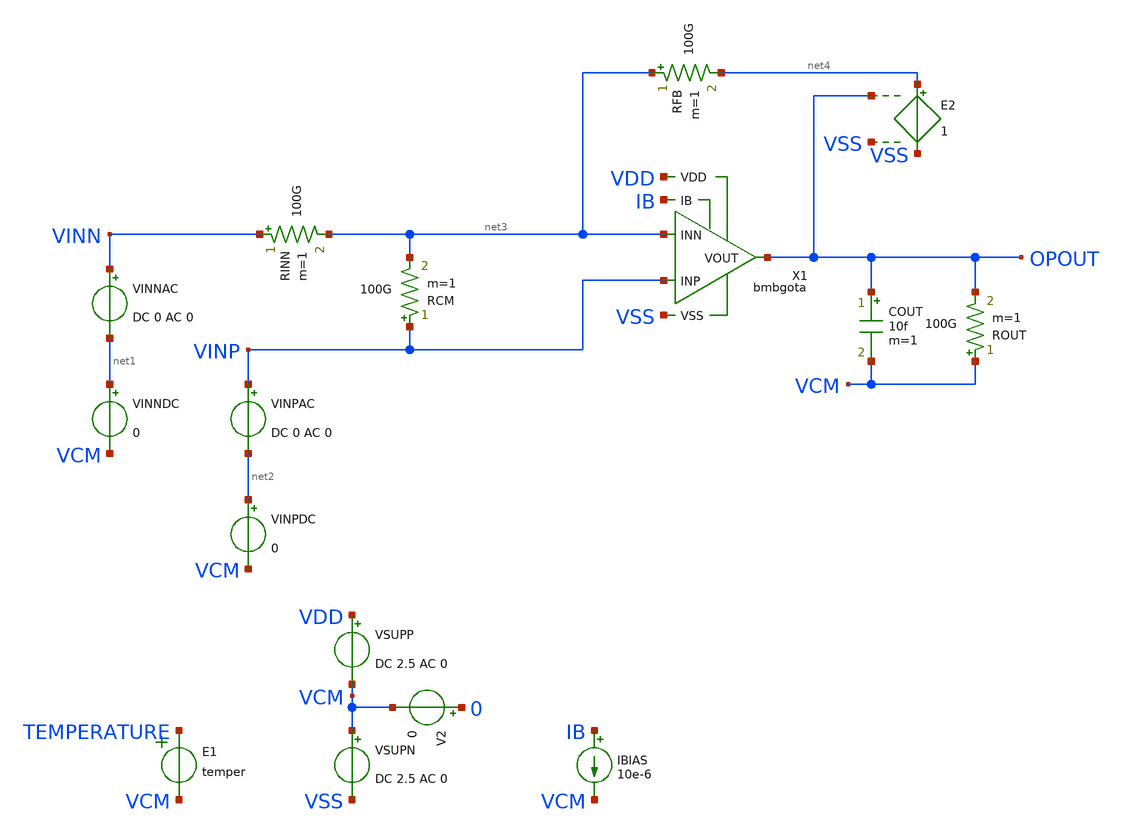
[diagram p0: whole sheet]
** sch_path: tt08/ip/bmbg/xschem/bmbgota_tb.sch
**.subckt bmbgota_tb
V2 0 VCM 0
E1 TEMPERATURE VCM VOL=' temper '
X1 VDD VSS OPOUT IB net3 VINP bmbgota
IBIAS IB VCM 10e-6
COUT OPOUT VCM 10f m=1
VINNDC net1 VCM 0
VINNAC VINN net1 DC 0 AC 0
VINPDC net2 VCM 0
VINPAC VINP net2 DC 0 AC 0
ROUT VCM OPOUT 100G m=1
VSUPP VDD VCM DC 2.5 AC 0
RFB net3 net4 100G m=1
RINN VINN net3 100G m=1
RCM VINP net3 100G m=1
VSUPN VCM VSS DC 2.5 AC 0
E2 net4 VSS OPOUT VSS 1
**** begin user architecture code

.csparam TB_ID=$::TB_ID\
.csparam MC_RUNS=$::MC_RUNS\
.csparam EXIT_NGSPICE=$::EXIT_NGSPICE\
.lib $::SKYWATER_MODELS/sky130.lib.spice $::CORNER\


* this experimental option enables mos model bin
* selection based on W/NF instead of W
.option wnflag=0

.control
* option savecurrents

* dummy block for goto
if (1)
if TB_ID = 0
	goto AC_OL
end
if TB_ID = 1
	goto AC_OL
end
if TB_ID = 2
	goto AC_CMRR_PSRR
end
if TB_ID = 3
	goto TRAN_OUTRNG
end
if TB_ID = 4
	goto TRAN_CMINP
end
if TB_ID = 5
	goto TRAN_SLEW
end
if TB_ID = 6
	goto AC_INOISE
end
if TB_ID = 7
	goto TRAN_THD
end

* Helper Functions
******************
define aunif(nom, avar) (nom+avar*sunif(0))
define agauss(nom, avar, sig) (nom + avar / sig * sgauss (0))

****************************************
label AC_OL
save all
****************************************
if MC_RUNS = 0
	let olgain_1hz = vector(MC_RUNS+1)
	let pm = vector(MC_RUNS+1)
	let ugbw = vector(MC_RUNS+1)
	let f1_3db = vector(MC_RUNS+1)
	let f2_3db = vector(MC_RUNS+1)
	let run=0

	.include ac_ol_ops.inc

	set nobreak
	set width=300
	print col olgain_1hz, pm, ugbw, f1_3db, f2_3db > ac_ol.csv
else
	let olgain_1hz = vector(MC_RUNS)
	let pm = vector(MC_RUNS)
	let ugbw = vector(MC_RUNS)
	let f1_3db = vector(MC_RUNS)
	let f2_3db = vector(MC_RUNS)
	let run=0
	dowhile run < MC_RUNS
		echo MC-RUN: $&run

		.include ac_ol_ops.inc

 		reset
		let run = run + 1
	end
	set nobreak
	set width=300
	print olgain_1hz, pm, ugbw, f1_3db, f2_3db > ac_ol.csv
end
goto done

****************************************
label AC_CMRR_PSRR
save all
****************************************
if MC_RUNS = 0
	let cmrr_10Hz = vector(MC_RUNS+1)
	let cmrr_10MHz = vector(MC_RUNS+1)
	let psrr_p_10Hz = vector(MC_RUNS+1)
	let psrr_p_10MHz = vector(MC_RUNS+1)
	let psrr_n_10Hz = vector(MC_RUNS+1)
	let psrr_n_10MHz = vector(MC_RUNS+1)
	let run=0

	.include ac_cmrr_psrr_ops.inc

	set nobreak
	set width=300
	print col cmrr_10Hz, cmrr_10MHz, psrr_p_10Hz, psrr_p_10MHz, psrr_n_10Hz, psrr_n_10MHz >
+ ac_cmrr_psrr.csv
else
	let cmrr_10Hz = vector(MC_RUNS)
	let cmrr_10MHz = vector(MC_RUNS)
	let psrr_p_10Hz = vector(MC_RUNS)
	let psrr_p_10MHz = vector(MC_RUNS)
	let psrr_n_10Hz = vector(MC_RUNS)
	let psrr_n_10MHz = vector(MC_RUNS)
	let run=0
	dowhile run < MC_RUNS
		echo MC-RUN: $&run

		.include ac_cmrr_psrr_ops.inc

 		reset
		let run = run + 1
	end
	set nobreak
	set width=300
	print cmrr_10Hz, cmrr_10MHz, psrr_p_10Hz, psrr_p_10MHz, psrr_n_10Hz, psrr_n_10MHz >
+ ac_cmrr_psrr.csv
end
goto done

****************************************
label TRAN_OUTRNG
save all
****************************************
if MC_RUNS = 0
	let neg_out_comp = vector(MC_RUNS+1)
	let pos_out_comp = vector(MC_RUNS+1)
	let run=0

	.include tran_outrng_ops.inc

	set nobreak
	set width=300
	print col neg_out_comp, pos_out_comp > tran_outrng.csv
else
	let neg_out_comp = vector(MC_RUNS)
	let pos_out_comp = vector(MC_RUNS)
	let run=0
	dowhile run < MC_RUNS
		echo MC-RUN: $&run

		.include tran_outrng_ops.inc

 		reset
		let run = run + 1
	end
	set nobreak
	set width=300
	print neg_out_comp, pos_out_comp > tran_outrng.csv
end
goto done

****************************************
label TRAN_CMINP
save all
****************************************
if MC_RUNS = 0
	let pos_cm_bound = vector(MC_RUNS+1)
	let neg_cm_bound = vector(MC_RUNS+1)
	let run=0

	.include tran_cminp_ops.inc

	set nobreak
	set width=300
	print col pos_cm_bound, neg_cm_bound > tran_inprng.csv
else
	let pos_cm_bound = vector(MC_RUNS)
	let neg_cm_bound = vector(MC_RUNS)
	let run=0
	dowhile run < MC_RUNS
		echo MC-RUN: $&run

		.include tran_cminp_ops.inc

 		reset
		let run = run + 1
	end
	set nobreak
	set width=300
	print pos_cm_bound, neg_cm_bound > tran_inprng.csv
end
goto done

****************************************
label TRAN_SLEW
save all
****************************************
if MC_RUNS = 0
	let inp_offset = vector(MC_RUNS+1)
	let slew_pos = vector(MC_RUNS+1)
	let slew_neg = vector(MC_RUNS+1)
	let run=0

	.include tran_slew_ops.inc

	set nobreak
	set width=300
	print col inp_offset, slew_pos, slew_neg > tran_slew.csv
else
	let inp_offset = vector(MC_RUNS)
	let slew_pos = vector(MC_RUNS)
	let slew_neg = vector(MC_RUNS)
	let run=0
	dowhile run < MC_RUNS
		echo MC-RUN: $&run

		.include tran_slew_ops.inc

 		reset
		let run = run + 1
	end
	set nobreak
	set width=300
	print inp_offset, slew_pos, slew_neg > tran_slew.csv
end
goto done

****************************************
label AC_INOISE
****************************************
alter vsupp dc = 2.5
alter vsupp ac = 0
alter vsupn dc = 2.5
alter vsupn ac = 0
alter vinnac ac = 0
alter vinndc dc = 0
alter vinpac ac = 0
alter vinpdc dc = 0
alter rinn resistance = 100e12
alter rinn ac = 100e12
alter rcm resistance = 100e12
alter rcm ac = 100e12
alter rfb resistance = 0
alter rfb ac = 0.01

noise v(opout) vinpac dec 10 1 100e6 1
print noise2.onoise_total noise2.inoise_total
plot noise1.onoise_spectrum
plot noise1.inoise_spectrum
setplot noise1
write noise1_opout.raw all

* https://sourceforge.net/p/ngspice/discussion/120973/thread/2aa3e30f/ -- Holger Vogt
* script to read a specific y-value if x given
**********************************************
let f0 = vector(1)
let f1 = vector(1)
let n_f0 = vector(1)
let n_f1 = vector(1)
compose freq_list values 10 10e3
foreach freq_idx 0 1
	let freq = freq_list[$freq_idx]
	* find index where freqency is just above interesting value
	setplot noise1
	let nn = 0
	while frequency[nn] < freq
		let nn = nn + 1
	end
	* define vectors of frequncies and values just above and below
	* selected frequeny
	let fnn = frequency[nn]
	let nn1 = nn - 1
	let fnn1 = frequency[nn1]
	let snn = onoise_spectrum[nn]
	let snn1 = onoise_spectrum[nn1]
	*print vector values
	echo nn = $&nn  fnn = $&fnn  snn = $&snn
	echo nn1 = $&nn1  fnn1 = $&fnn1  snn1 = $&snn1
	*linear interpolation for exact frequency
	let newsnn = snn1 + (snn - snn1)/(fnn - fnn1)*(freq - fnn1)
	echo newfnn = $&freq  newsnn = $&newsnn
	if $freq_idx = 0
		let f0 = freq
		let n_f0 = newsnn
	end
	if $freq_idx = 1
		let f1 = freq
		let n_f1 = newsnn
	end
end
set nobreak
set width=300
set noprintscale
print col f0, n_f0, f1, n_f1 > ac_inoise.csv

goto done

****************************************
label TRAN_THD
save all
****************************************
if MC_RUNS = 0
	let thd = vector(MC_RUNS+1)
	let run=0

	.include tran_thd_ops.inc

	set nobreak
	set width=300
	print col thd > tran_thd.csv
else
	let thd = vector(MC_RUNS)
	let run=0
	dowhile run < MC_RUNS
		echo MC-RUN: $&run

		reset

		.include tran_thd_ops.inc

		let run = run + 1
	end
	set nobreak
	set width=300
	print thd > tran_thd.csv
end
goto done

****************************************
label done
****************************************
if EXIT_NGSPICE > 0.0
	exit
end
end
.endc


**** end user architecture code
**.ends

* expanding   symbol:  bmbgota.sym # of pins=6
** sym_path: bmbgota.sym
** sch_path: bmbgota.sch
.subckt bmbgota VDD VSS VOUT IB INN INP
*.iopin INP
*.iopin INN
*.iopin VOUT
*.opin IB
*.iopin VDD
*.iopin VSS
XMDR vr INP vt VDD sky130_fd_pr__pfet_g5v0d10v5 L=1 W=20 nf=1 ad='int((nf+1)/2) * W/nf * 0.29' as='int((nf+2)/2) * W/nf * 0.29'
+ pd='2*int((nf+1)/2) * (W/nf + 0.29)' ps='2*int((nf+2)/2) * (W/nf + 0.29)' nrd='0.29 / W' nrs='0.29 / W'
+ sa=0 sb=0 sd=0 mult=8 m=8
XMMIRL vl vl VSS VSS sky130_fd_pr__nfet_g5v0d10v5 L=2 W=5 nf=1 ad='int((nf+1)/2) * W/nf * 0.29' as='int((nf+2)/2) * W/nf * 0.29'
+ pd='2*int((nf+1)/2) * (W/nf + 0.29)' ps='2*int((nf+2)/2) * (W/nf + 0.29)' nrd='0.29 / W' nrs='0.29 / W'
+ sa=0 sb=0 sd=0 mult=4 m=4
XMMIRR vr vl VSS VSS sky130_fd_pr__nfet_g5v0d10v5 L=2 W=5 nf=1 ad='int((nf+1)/2) * W/nf * 0.29' as='int((nf+2)/2) * W/nf * 0.29'
+ pd='2*int((nf+1)/2) * (W/nf + 0.29)' ps='2*int((nf+2)/2) * (W/nf + 0.29)' nrd='0.29 / W' nrs='0.29 / W'
+ sa=0 sb=0 sd=0 mult=4 m=4
XMDL vl INN vt VDD sky130_fd_pr__pfet_g5v0d10v5 L=1 W=20 nf=1 ad='int((nf+1)/2) * W/nf * 0.29' as='int((nf+2)/2) * W/nf * 0.29'
+ pd='2*int((nf+1)/2) * (W/nf + 0.29)' ps='2*int((nf+2)/2) * (W/nf + 0.29)' nrd='0.29 / W' nrs='0.29 / W'
+ sa=0 sb=0 sd=0 mult=8 m=8
XMMIR2 vt IB VDD VDD sky130_fd_pr__pfet_g5v0d10v5 L=2 W=5 nf=1 ad='int((nf+1)/2) * W/nf * 0.29' as='int((nf+2)/2) * W/nf * 0.29'
+ pd='2*int((nf+1)/2) * (W/nf + 0.29)' ps='2*int((nf+2)/2) * (W/nf + 0.29)' nrd='0.29 / W' nrs='0.29 / W'
+ sa=0 sb=0 sd=0 mult=2 m=2
XMMIR1 IB IB VDD VDD sky130_fd_pr__pfet_g5v0d10v5 L=2 W=5 nf=1 ad='int((nf+1)/2) * W/nf * 0.29' as='int((nf+2)/2) * W/nf * 0.29'
+ pd='2*int((nf+1)/2) * (W/nf + 0.29)' ps='2*int((nf+2)/2) * (W/nf + 0.29)' nrd='0.29 / W' nrs='0.29 / W'
+ sa=0 sb=0 sd=0 mult=1 m=1
XMO VOUT vr VSS VSS sky130_fd_pr__nfet_g5v0d10v5 L=2 W=5 nf=1 ad='int((nf+1)/2) * W/nf * 0.29' as='int((nf+2)/2) * W/nf * 0.29'
+ pd='2*int((nf+1)/2) * (W/nf + 0.29)' ps='2*int((nf+2)/2) * (W/nf + 0.29)' nrd='0.29 / W' nrs='0.29 / W'
+ sa=0 sb=0 sd=0 mult=4 m=4
XMMIR3 VOUT IB VDD VDD sky130_fd_pr__pfet_g5v0d10v5 L=2 W=5 nf=1 ad='int((nf+1)/2) * W/nf * 0.29' as='int((nf+2)/2) * W/nf * 0.29'
+ pd='2*int((nf+1)/2) * (W/nf + 0.29)' ps='2*int((nf+2)/2) * (W/nf + 0.29)' nrd='0.29 / W' nrs='0.29 / W'
+ sa=0 sb=0 sd=0 mult=3 m=3
XR1 net1 vr VSS sky130_fd_pr__res_xhigh_po_1p41 L=7 mult=1 m=1
XC1 net1 VOUT sky130_fd_pr__cap_mim_m3_1 W=16 L=30 MF=1 m=1
XMDL1 VDD VDD VDD VDD sky130_fd_pr__pfet_g5v0d10v5 L=1 W=20 nf=1 ad='int((nf+1)/2) * W/nf * 0.29' as='int((nf+2)/2) * W/nf * 0.29'
+ pd='2*int((nf+1)/2) * (W/nf + 0.29)' ps='2*int((nf+2)/2) * (W/nf + 0.29)' nrd='0.29 / W' nrs='0.29 / W'
+ sa=0 sb=0 sd=0 mult=1 m=1
XMDR1 VDD VDD VDD VDD sky130_fd_pr__pfet_g5v0d10v5 L=1 W=20 nf=1 ad='int((nf+1)/2) * W/nf * 0.29' as='int((nf+2)/2) * W/nf * 0.29'
+ pd='2*int((nf+1)/2) * (W/nf + 0.29)' ps='2*int((nf+2)/2) * (W/nf + 0.29)' nrd='0.29 / W' nrs='0.29 / W'
+ sa=0 sb=0 sd=0 mult=1 m=1
XMMIRL1 VSS VSS VSS VSS sky130_fd_pr__nfet_g5v0d10v5 L=2 W=5 nf=1 ad='int((nf+1)/2) * W/nf * 0.29' as='int((nf+2)/2) * W/nf * 0.29'
+ pd='2*int((nf+1)/2) * (W/nf + 0.29)' ps='2*int((nf+2)/2) * (W/nf + 0.29)' nrd='0.29 / W' nrs='0.29 / W'
+ sa=0 sb=0 sd=0 mult=1 m=1
XMMIRR1 VSS VSS VSS VSS sky130_fd_pr__nfet_g5v0d10v5 L=2 W=5 nf=1 ad='int((nf+1)/2) * W/nf * 0.29' as='int((nf+2)/2) * W/nf * 0.29'
+ pd='2*int((nf+1)/2) * (W/nf + 0.29)' ps='2*int((nf+2)/2) * (W/nf + 0.29)' nrd='0.29 / W' nrs='0.29 / W'
+ sa=0 sb=0 sd=0 mult=1 m=1
.ends

.end
